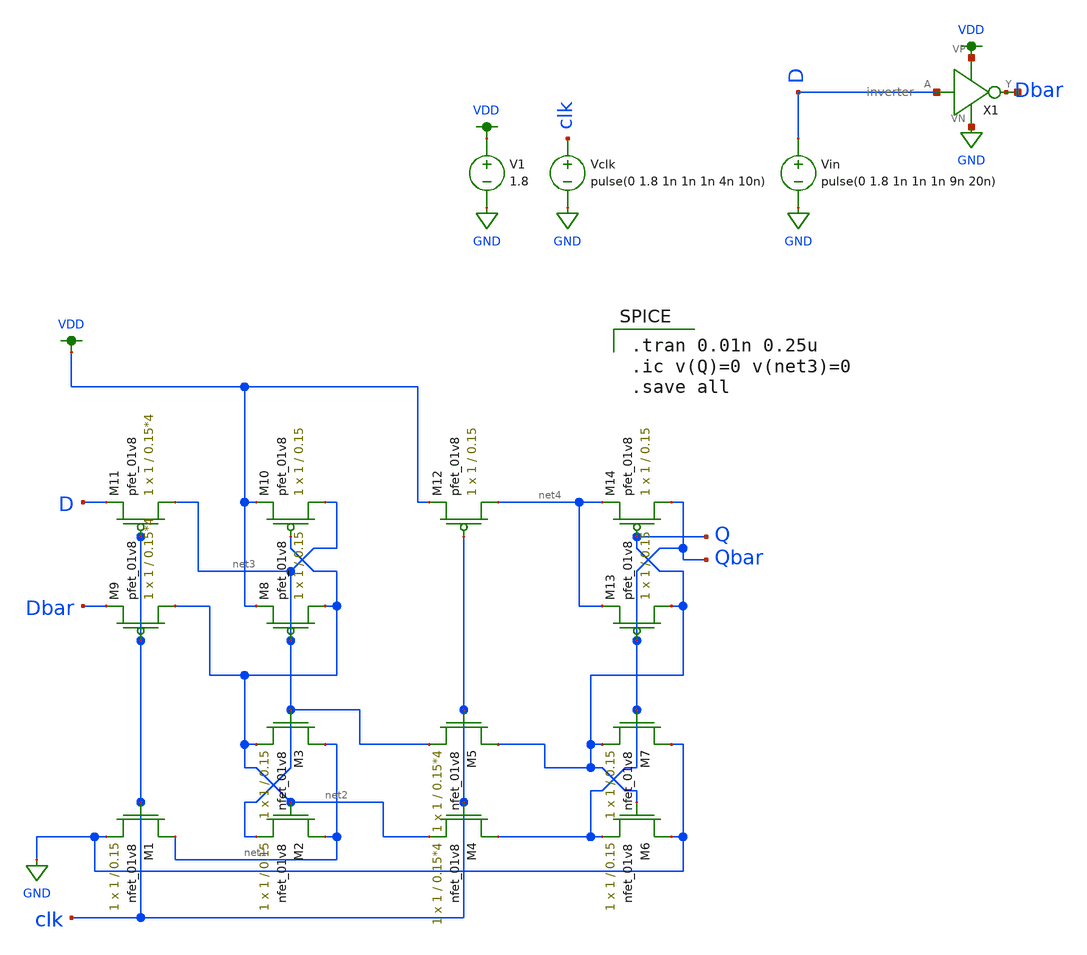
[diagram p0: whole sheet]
** sch_path: dff_test.sch
**.subckt dff_test
XM1 net1 clk GND GND sky130_fd_pr__nfet_01v8 L=0.15 W=1 nf=1 ad='int((nf+1)/2) * W/nf * 0.29' as='int((nf+2)/2) * W/nf * 0.29'
+ pd='2*int((nf+1)/2) * (W/nf + 0.29)' ps='2*int((nf+2)/2) * (W/nf + 0.29)' nrd='0.29 / W' nrs='0.29 / W'
+ sa=0 sb=0 sd=0 mult=1 m=1
XM2 net1 net2 net3 GND sky130_fd_pr__nfet_01v8 L=0.15 W=1 nf=1 ad='int((nf+1)/2) * W/nf * 0.29' as='int((nf+2)/2) * W/nf * 0.29'
+ pd='2*int((nf+1)/2) * (W/nf + 0.29)' ps='2*int((nf+2)/2) * (W/nf + 0.29)' nrd='0.29 / W' nrs='0.29 / W'
+ sa=0 sb=0 sd=0 mult=1 m=1
XM3 net1 net3 net2 GND sky130_fd_pr__nfet_01v8 L=0.15 W=1 nf=1 ad='int((nf+1)/2) * W/nf * 0.29' as='int((nf+2)/2) * W/nf * 0.29'
+ pd='2*int((nf+1)/2) * (W/nf + 0.29)' ps='2*int((nf+2)/2) * (W/nf + 0.29)' nrd='0.29 / W' nrs='0.29 / W'
+ sa=0 sb=0 sd=0 mult=1 m=1
XM4 Qbar clk net2 GND sky130_fd_pr__nfet_01v8 L=0.15*4 W=1 nf=1 ad='int((nf+1)/2) * W/nf * 0.29' as='int((nf+2)/2) * W/nf * 0.29'
+ pd='2*int((nf+1)/2) * (W/nf + 0.29)' ps='2*int((nf+2)/2) * (W/nf + 0.29)' nrd='0.29 / W' nrs='0.29 / W'
+ sa=0 sb=0 sd=0 mult=1 m=1
XM5 Q clk net3 GND sky130_fd_pr__nfet_01v8 L=0.15*4 W=1 nf=1 ad='int((nf+1)/2) * W/nf * 0.29' as='int((nf+2)/2) * W/nf * 0.29'
+ pd='2*int((nf+1)/2) * (W/nf + 0.29)' ps='2*int((nf+2)/2) * (W/nf + 0.29)' nrd='0.29 / W' nrs='0.29 / W'
+ sa=0 sb=0 sd=0 mult=1 m=1
XM6 GND Q Qbar GND sky130_fd_pr__nfet_01v8 L=0.15 W=1 nf=1 ad='int((nf+1)/2) * W/nf * 0.29' as='int((nf+2)/2) * W/nf * 0.29'
+ pd='2*int((nf+1)/2) * (W/nf + 0.29)' ps='2*int((nf+2)/2) * (W/nf + 0.29)' nrd='0.29 / W' nrs='0.29 / W'
+ sa=0 sb=0 sd=0 mult=1 m=1
XM7 GND Qbar Q GND sky130_fd_pr__nfet_01v8 L=0.15 W=1 nf=1 ad='int((nf+1)/2) * W/nf * 0.29' as='int((nf+2)/2) * W/nf * 0.29'
+ pd='2*int((nf+1)/2) * (W/nf + 0.29)' ps='2*int((nf+2)/2) * (W/nf + 0.29)' nrd='0.29 / W' nrs='0.29 / W'
+ sa=0 sb=0 sd=0 mult=1 m=1
XM8 net2 net3 VDD VDD sky130_fd_pr__pfet_01v8 L=0.15 W=1 nf=1 ad='int((nf+1)/2) * W/nf * 0.29' as='int((nf+2)/2) * W/nf * 0.29'
+ pd='2*int((nf+1)/2) * (W/nf + 0.29)' ps='2*int((nf+2)/2) * (W/nf + 0.29)' nrd='0.29 / W' nrs='0.29 / W'
+ sa=0 sb=0 sd=0 mult=1 m=1
XM9 net2 clk Dbar VDD sky130_fd_pr__pfet_01v8 L=0.15*4 W=1 nf=1 ad='int((nf+1)/2) * W/nf * 0.29' as='int((nf+2)/2) * W/nf * 0.29'
+ pd='2*int((nf+1)/2) * (W/nf + 0.29)' ps='2*int((nf+2)/2) * (W/nf + 0.29)' nrd='0.29 / W' nrs='0.29 / W'
+ sa=0 sb=0 sd=0 mult=1 m=1
XM10 net3 net2 VDD VDD sky130_fd_pr__pfet_01v8 L=0.15 W=1 nf=1 ad='int((nf+1)/2) * W/nf * 0.29' as='int((nf+2)/2) * W/nf * 0.29'
+ pd='2*int((nf+1)/2) * (W/nf + 0.29)' ps='2*int((nf+2)/2) * (W/nf + 0.29)' nrd='0.29 / W' nrs='0.29 / W'
+ sa=0 sb=0 sd=0 mult=1 m=1
XM11 net3 clk D VDD sky130_fd_pr__pfet_01v8 L=0.15*4 W=1 nf=1 ad='int((nf+1)/2) * W/nf * 0.29' as='int((nf+2)/2) * W/nf * 0.29'
+ pd='2*int((nf+1)/2) * (W/nf + 0.29)' ps='2*int((nf+2)/2) * (W/nf + 0.29)' nrd='0.29 / W' nrs='0.29 / W'
+ sa=0 sb=0 sd=0 mult=1 m=1
XM12 net4 clk VDD VDD sky130_fd_pr__pfet_01v8 L=0.15 W=1 nf=1 ad='int((nf+1)/2) * W/nf * 0.29' as='int((nf+2)/2) * W/nf * 0.29'
+ pd='2*int((nf+1)/2) * (W/nf + 0.29)' ps='2*int((nf+2)/2) * (W/nf + 0.29)' nrd='0.29 / W' nrs='0.29 / W'
+ sa=0 sb=0 sd=0 mult=1 m=1
XM13 Q Qbar net4 VDD sky130_fd_pr__pfet_01v8 L=0.15 W=1 nf=1 ad='int((nf+1)/2) * W/nf * 0.29' as='int((nf+2)/2) * W/nf * 0.29'
+ pd='2*int((nf+1)/2) * (W/nf + 0.29)' ps='2*int((nf+2)/2) * (W/nf + 0.29)' nrd='0.29 / W' nrs='0.29 / W'
+ sa=0 sb=0 sd=0 mult=1 m=1
XM14 Qbar Q net4 VDD sky130_fd_pr__pfet_01v8 L=0.15 W=1 nf=1 ad='int((nf+1)/2) * W/nf * 0.29' as='int((nf+2)/2) * W/nf * 0.29'
+ pd='2*int((nf+1)/2) * (W/nf + 0.29)' ps='2*int((nf+2)/2) * (W/nf + 0.29)' nrd='0.29 / W' nrs='0.29 / W'
+ sa=0 sb=0 sd=0 mult=1 m=1
V1 VDD GND 1.8
Vclk clk GND pulse(0 1.8 1n 1n 1n 4n 10n)
Vin D GND pulse(0 1.8 1n 1n 1n 9n 20n)
X1 D net5 VDD GND inverter
**** begin user architecture code

.tran 0.01n 0.25u
.ic v(Q)=0 v(net3)=0
.save all


.option wnflag=1
.lib ~/skywater/skywater-pdk/libraries/sky130_fd_pr_ngspice/latest/models/sky130.lib.spice tt

**** end user architecture code
**.ends

* expanding   symbol:  /home/jonah/VLSI/MP1/inverter.sym # of pins=4
** sym_path: /home/jonah/VLSI/MP1/inverter.sym
** sch_path: /home/jonah/VLSI/MP1/inverter.sch
.subckt inverter A Y VP VN
*.ipin A
*.iopin VP
*.iopin VN
*.iopin Y
XM1 Y A VN VN sky130_fd_pr__nfet_01v8 L=0.15 W=1 nf=1 ad='int((nf+1)/2) * W/nf * 0.29' as='int((nf+2)/2) * W/nf * 0.29'
+ pd='2*int((nf+1)/2) * (W/nf + 0.29)' ps='2*int((nf+2)/2) * (W/nf + 0.29)' nrd='0.29 / W' nrs='0.29 / W'
+ sa=0 sb=0 sd=0 mult=1 m=1
XM2 Y A VP VP sky130_fd_pr__pfet_01v8 L=0.15 W=1 nf=1 ad='int((nf+1)/2) * W/nf * 0.29' as='int((nf+2)/2) * W/nf * 0.29'
+ pd='2*int((nf+1)/2) * (W/nf + 0.29)' ps='2*int((nf+2)/2) * (W/nf + 0.29)' nrd='0.29 / W' nrs='0.29 / W'
+ sa=0 sb=0 sd=0 mult=1 m=1
.ends

.GLOBAL VDD
.GLOBAL GND
.end
